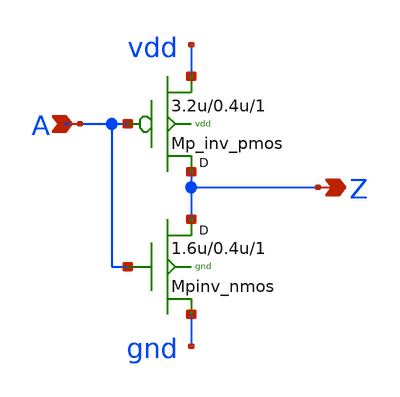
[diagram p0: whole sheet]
** sch_path: sram_2_64_scn4m_lcc/pinv_0.sch
**.subckt pinv_0 A Z
*.ipin A
*.opin Z
Mpinv_nmos Z A gnd gnd n w=1.6u l=0.4u m=1
Mp_inv_pmos Z A vdd vdd p w=3.2u l=0.4u m=1
**.ends
.end
